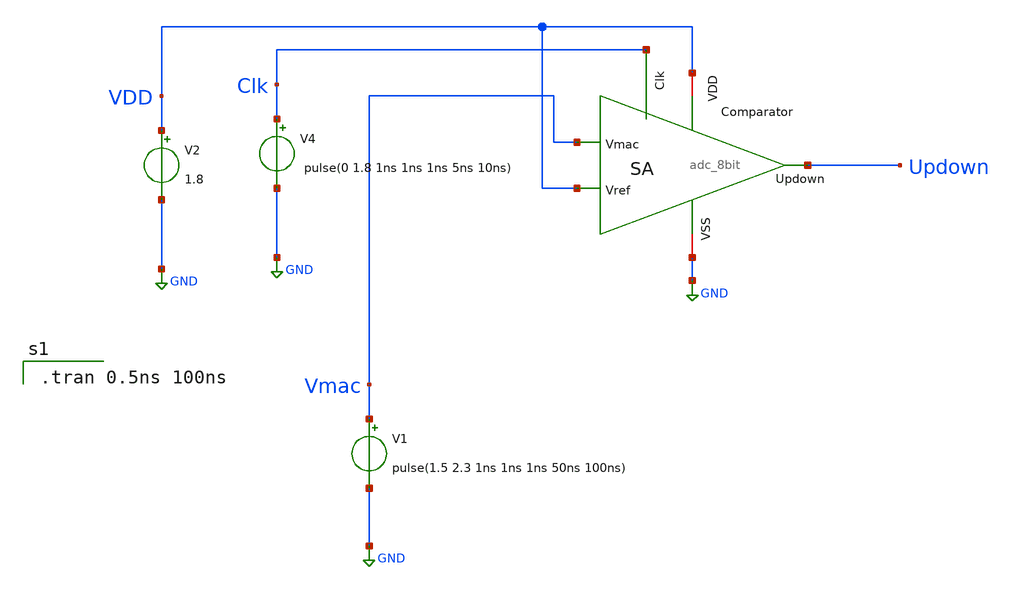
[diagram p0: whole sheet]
** sch_path: ADC_schematics/adc_comp/sim_adc_8bit.sch
**.subckt sim_adc_8bit
x1 GND VDD VDD Clk Vmac Updown adc_8bit
V2 VDD GND 1.8
V1 Vmac GND pulse(1.5 2.3 1ns 1ns 1ns 50ns 100ns)
V4 Clk GND pulse(0 1.8 1ns 1ns 1ns 5ns 10ns)
**** begin user architecture code

.tran 0.5ns 100ns


** opencircuitdesign pdks install
.lib $::SKYWATER_MODELS/sky130.lib.spice tt
.include $::SKYWATER_STDCELLS/sky130_fd_sc_hd.spice

**** end user architecture code
**.ends
.GLOBAL GND
.end
